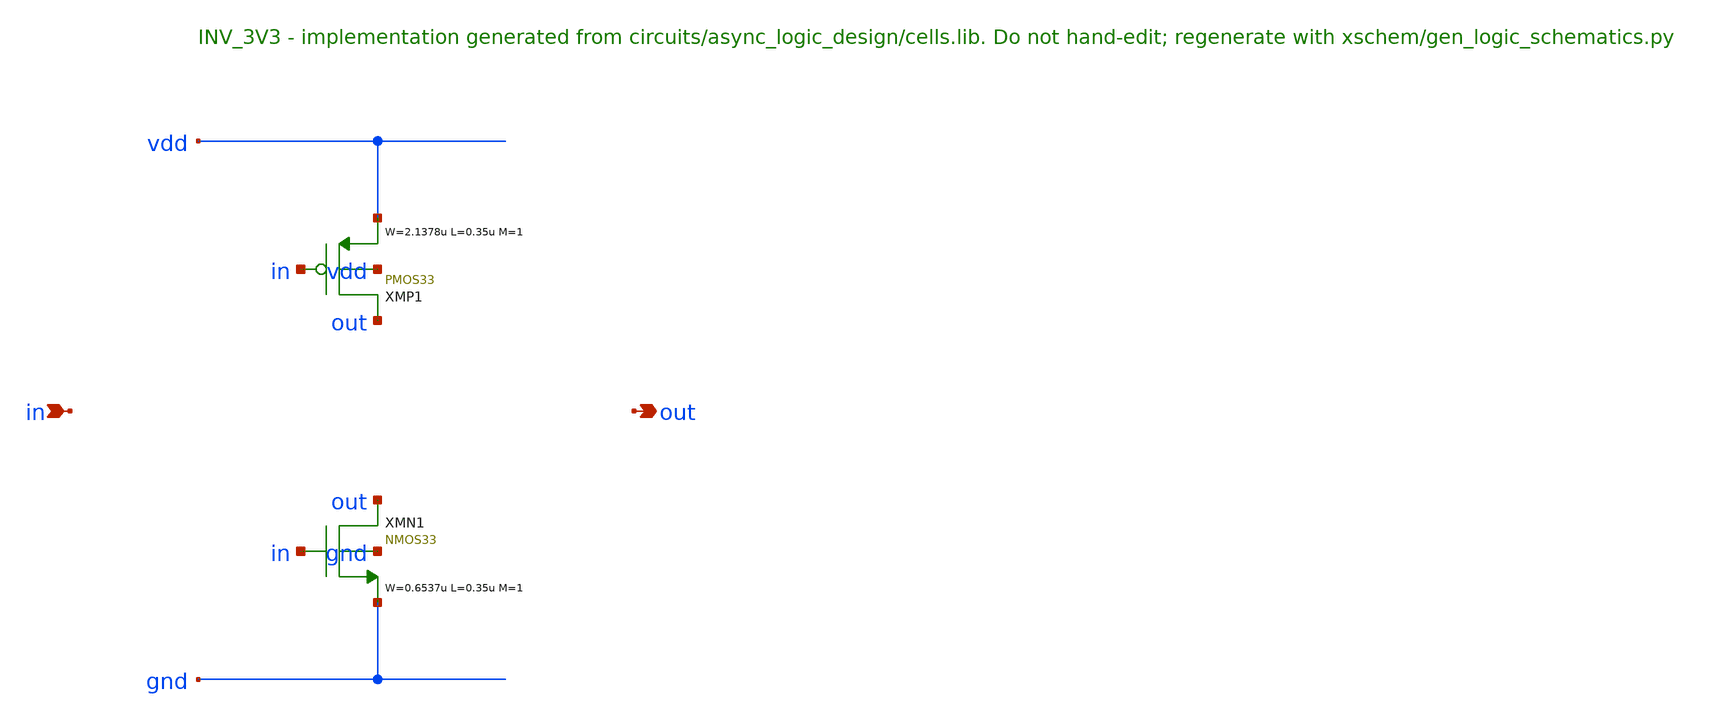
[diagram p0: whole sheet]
** sch_path: xschem/logic/INV_3V3.sch
**.subckt INV_3V3 in out
*.ipin in
*.opin out
XMP1 out in vdd vdd PMOS33 W=2.1378u L=0.35u M=1 MM_SIGMA=0
XMN1 out in gnd gnd NMOS33 W=0.6537u L=0.35u M=1 MM_SIGMA=0
**.ends
.end
